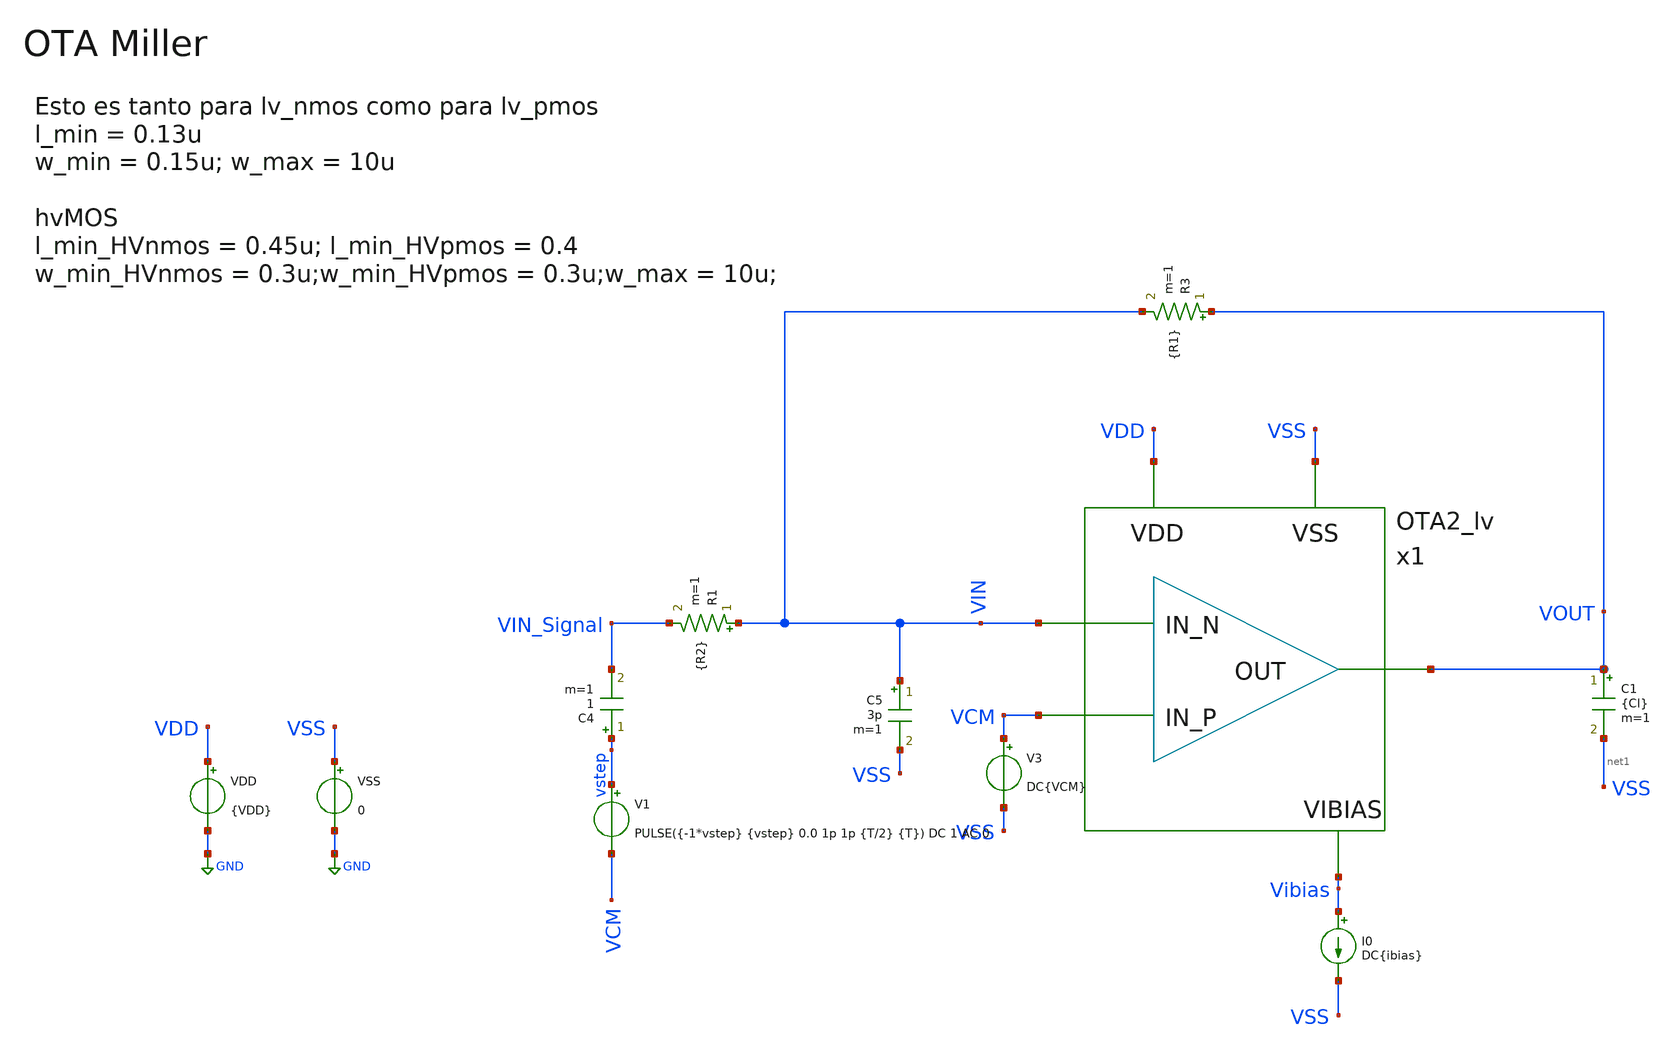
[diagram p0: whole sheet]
** sch_path: xschem/Ayudantias/Ayudantia_2/TB_OTA2_StepResp.sch
**.subckt TB_OTA2_StepResp
VDD VDD GND {VDD}
I0 Vibias VSS DC{ibias}
R3 VOUT VIN {R1} m=1
V3 VCM VSS DC{VCM}
VSS VSS GND 0
C5 VIN VSS 3p m=1
R1 VIN VIN_Signal {R2} m=1
C1 VOUT net1 {Cl} m=1
C4 vstep VIN_Signal 1 m=1
x1 VIN VCM VOUT VDD VSS Vibias OTA2_lv
V1 vstep VCM PULSE({-1*vstep} {vstep} 0.0 1p 1p {T/2} {T}) DC 1 AC 0
**** begin user architecture code


*.param VDD = 3.3
.param VDD = 1.2
.param VCM = 0.6
.param Ibias = 100u
.param Pi = 3.14159265
.param wo = 2*Pi*60Meg
.csparam wo = {wo}

.param VAC = 10m
*.param VAC  = 30m
*.param fin  = 9.765625e5
.param fin  = 1e4
.param T = 1/fin

.param vstep = 10m

.param R1 = 100k
*.param R2 = R1/10
.param R2 = R1/30

*.ic v(Vo) = 0

* OP Parameters & Singals to save
.save all

*.option temp = 125
*.option temp = -40
.option temp = 27





.lib cornerMOShv.lib mos_tt
.lib cornerMOSlv.lib mos_tt
*.lib cornerMOShv.lib mos_ff
*.lib cornerMOSlv.lib mos_ff
*.lib cornerMOShv.lib mos_ss
*.lib cornerMOSlv.lib mos_ss
*.lib cornerMOShv.lib mos_sf
*.lib cornerMOSlv.lib mos_sf
*.lib cornerMOShv.lib mos_fs
*.lib cornerMOSlv.lib mos_fs

.include /opt/pdks/ihp-sg13g2/libs.ref/sg13g2_stdcell/spice/sg13g2_stdcell.spice
.lib $::SG13G2_MODELS/cornerRES.lib res_typ
.lib $::SG13G2_MODELS/cornerCAP.lib cap_typ
*.lib $::SG13G2_MODELS/diodes.lib




*.param SimTime = 10*T
*.tran 0.01u {SimTime} uic
*.save all v(vsen)
.control

  set color0 = white
  tran 0.1u 100u
  setplot tran1
  *plot v(vsen) v(VOUT)
  plot v(vstep) v(VIN_signal) v(VOUT)
.endc

.end




.param temp=27

.param m_M8 = 200
.param m_M7 = 18
.param m_M5 = 4500
.param w_M8 =1u
.param w_M7 =1u
.param w_M5 =1u
.param l_M875 = 1u

.param m_M12 = 3
.param w_M12 =1u
.param l_M12 = 1u

.param m_M34 = 4
.param w_M34 =1u
.param l_M34 = 9u

.param m_M6 = 420
.param w_M6 =1u
.param l_M6 = 1u

.param m_R = 1
*.param w_R =10u
.param w_R = 0.15u
.param l_R = 0.13u

*.param Cc = 0.1p
.param Cc = 0.4p
.param Cl = 20p
.csparam Cl = {Cl}
.csparam Cc = {Cc}






**** end user architecture code
**.ends

* expanding   symbol:
*+  /workspaces/usm-vlsi-tools/shared_xserver/simulations/Projects/IHP/IPD413_202501/xschem/Tareas/Tarea_2/OTA2_lv.sym # of pins=6
** sym_path: xschem/Ayudantias/Ayudantia_2/OTA2_lv.sym
** sch_path: xschem/Ayudantias/Ayudantia_2/OTA2_lv.sch
.subckt OTA2_lv IN_N IN_P OUT VDD VSS Vibias
*.ipin IN_N
*.ipin IN_P
*.ipin Vibias
*.opin OUT
*.iopin VDD
*.iopin VSS
XM1 VB IN_N net1 VA sg13_lv_pmos w={w_M12} l={l_M12} ng=1 m={m_M12} mm_ok=1
XM3 VSS VB VB VSS sg13_lv_nmos w={w_M34} l={l_M34} ng=1 m={m_M34} mm_ok=1
XM2 VC IN_P net2 VA sg13_lv_pmos w={w_M12} l={l_M12} ng=1 m={m_M12} mm_ok=1
XM4 VSS VB net6 VSS sg13_lv_nmos w={w_M34} l={l_M34} ng=1 m={m_M34} mm_ok=1
XM5 net5 Vibias VDD VDD sg13_lv_pmos w={w_M5} l={l_M875} ng=1 m={m_M5} mm_ok=1
XM6 VSS VC net3 VSS sg13_lv_nmos w={w_M6} l={l_M6} ng=1 m={m_M6} mm_ok=1
XM7 net7 Vibias VDD VDD sg13_lv_pmos w={w_M7} l={l_M875} ng=1 m={m_M7} mm_ok=1
XM8 net8 Vibias VDD VDD sg13_lv_pmos w={w_M8} l={l_M875} ng=1 m={m_M8} mm_ok=1
XM9 VsMR VDD VC VSS sg13_lv_nmos w={w_R} l={l_R} ng=1 m={m_R} mm_ok=1
C1 VsMR net4 {Cc} m=1
Vmeas VA net1 0
.save i(vmeas)
Vmeas1 VC net6 0
.save i(vmeas1)
Vmeas2 VA net2 0
.save i(vmeas2)
Vmeas3 net4 net3 0
.save i(vmeas3)
Vmeas4 net5 net4 0
.save i(vmeas4)
Vmeas5 net7 VA 0
.save i(vmeas5)
Vmeas6 net8 Vibias 0
.save i(vmeas6)
Vmeas7 net4 OUT 0
.save i(vmeas7)
.ends

.GLOBAL GND
.end
